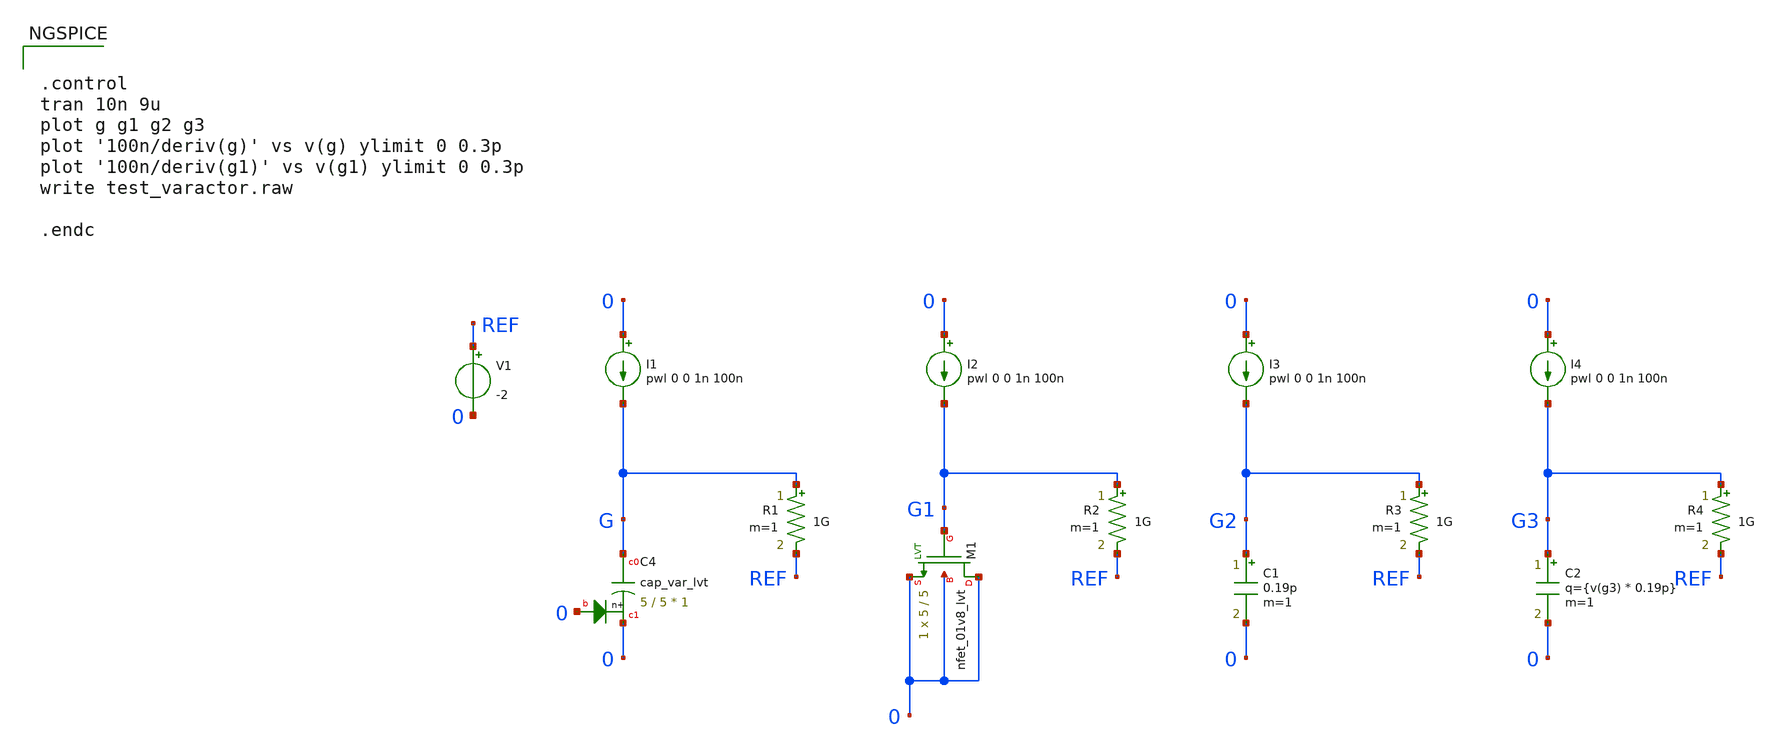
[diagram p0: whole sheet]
** sch_path: xyce/sky130A-xyce/libs.tech/xschem/sky130_tests/test_varactor.sch
* Copyright 2020 Stefan Frederik Schippers
* Licensed under the Apache License, Version 2.0 (the "License");
* you may not use this file except in compliance with the License.
* You may obtain a copy of the License at
* https://www.apache.org/licenses/LICENSE-2.0
* Unless required by applicable law or agreed to in writing, software
* distributed under the License is distributed on an "AS IS" BASIS,
* WITHOUT WARRANTIES OR CONDITIONS OF ANY KIND, either express or implied.
* See the License for the specific language governing permissions and
* limitations under the License.
**.subckt test_varactor
I1 0 G pwl 0 0 1n 100n
R1 G REF 1G m=1
I2 0 G1 pwl 0 0 1n 100n
R2 G1 REF 1G m=1
I3 0 G2 pwl 0 0 1n 100n
R3 G2 REF 1G m=1
C1 G2 0 0.19p m=1
V1 REF 0 -2
XM1 0 G1 0 0 sky130_fd_pr__nfet_01v8_lvt L=5 W=5 nf=1 ad='W * 0.29' as='W * 0.29' pd='2 * (W + 0.29)'
+ ps='2 * (W + 0.29)' nrd='0.29 / W' nrs='0.29 / W' sa=0 sb=0 sd=0 mult=1 m=1
I4 0 G3 pwl 0 0 1n 100n
R4 G3 REF 1G m=1
C2 G3 0 q={v(g3) * 0.19p} m=1
XC4 G 0 0 sky130_fd_pr__cap_var_lvt W=5 L=5 VM=1
**** begin user architecture code


.control
tran 10n 9u
plot g g1 g2 g3
plot '100n/deriv(g)' vs v(g) ylimit 0 0.3p
plot '100n/deriv(g1)' vs v(g1) ylimit 0 0.3p
write test_varactor.raw

.endc



.include $::SKYWATER_MODELS/cells/nfet_01v8/sky130_fd_pr__nfet_01v8__tt.corner.spice
.include $::SKYWATER_MODELS/cells/nfet_01v8_lvt/sky130_fd_pr__nfet_01v8_lvt__tt.corner.spice
.include $::SKYWATER_MODELS/cells/pfet_01v8/sky130_fd_pr__pfet_01v8__tt.corner.spice
.include $::SKYWATER_MODELS/cells/nfet_03v3_nvt/sky130_fd_pr__nfet_03v3_nvt__tt.corner.spice
.include $::SKYWATER_MODELS/cells/nfet_05v0_nvt/sky130_fd_pr__nfet_05v0_nvt__tt.corner.spice
.include $::SKYWATER_MODELS/cells/esd_nfet_01v8/sky130_fd_pr__esd_nfet_01v8__tt.corner.spice
.include $::SKYWATER_MODELS/cells/pfet_01v8_lvt/sky130_fd_pr__pfet_01v8_lvt__tt.corner.spice
.include $::SKYWATER_MODELS/cells/pfet_01v8_hvt/sky130_fd_pr__pfet_01v8_hvt__tt.corner.spice
.include $::SKYWATER_MODELS/cells/esd_pfet_g5v0d10v5/sky130_fd_pr__esd_pfet_g5v0d10v5__tt.corner.spice
.include $::SKYWATER_MODELS/cells/pfet_g5v0d10v5/sky130_fd_pr__pfet_g5v0d10v5__tt.corner.spice
.include $::SKYWATER_MODELS/cells/pfet_g5v0d16v0/sky130_fd_pr__pfet_g5v0d16v0__tt.corner.spice
.include $::SKYWATER_MODELS/cells/nfet_g5v0d10v5/sky130_fd_pr__nfet_g5v0d10v5__tt.corner.spice
.include $::SKYWATER_MODELS/cells/nfet_g5v0d16v0/sky130_fd_pr__nfet_g5v0d16v0__tt_discrete.corner.spice
.include $::SKYWATER_MODELS/cells/esd_nfet_g5v0d10v5/sky130_fd_pr__esd_nfet_g5v0d10v5__tt.corner.spice
.include $::SKYWATER_MODELS/models/corners/tt/nonfet.spice
* Mismatch parameters
.include $::SKYWATER_MODELS/cells/nfet_01v8/sky130_fd_pr__nfet_01v8__mismatch.corner.spice
.include $::SKYWATER_MODELS/cells/pfet_01v8/sky130_fd_pr__pfet_01v8__mismatch.corner.spice
.include $::SKYWATER_MODELS/cells/nfet_01v8_lvt/sky130_fd_pr__nfet_01v8_lvt__mismatch.corner.spice
.include $::SKYWATER_MODELS/cells/pfet_01v8_lvt/sky130_fd_pr__pfet_01v8_lvt__mismatch.corner.spice
.include $::SKYWATER_MODELS/cells/pfet_01v8_hvt/sky130_fd_pr__pfet_01v8_hvt__mismatch.corner.spice
.include $::SKYWATER_MODELS/cells/nfet_g5v0d10v5/sky130_fd_pr__nfet_g5v0d10v5__mismatch.corner.spice
.include $::SKYWATER_MODELS/cells/pfet_g5v0d10v5/sky130_fd_pr__pfet_g5v0d10v5__mismatch.corner.spice
.include $::SKYWATER_MODELS/cells/nfet_05v0_nvt/sky130_fd_pr__nfet_05v0_nvt__mismatch.corner.spice
.include $::SKYWATER_MODELS/cells/nfet_03v3_nvt/sky130_fd_pr__nfet_03v3_nvt__mismatch.corner.spice
* Resistor$::SKYWATER_MODELS/Capacitor
.include $::SKYWATER_MODELS/models/r+c/res_typical__cap_typical.spice
.include $::SKYWATER_MODELS/models/r+c/res_typical__cap_typical__lin.spice
* Special cells
.include $::SKYWATER_MODELS/models/corners/tt/specialized_cells.spice
* All models
.include $::SKYWATER_MODELS/models/all.spice
* Corner
.include $::SKYWATER_MODELS/models/corners/tt/rf.spice

**** end user architecture code
**.ends
.end
